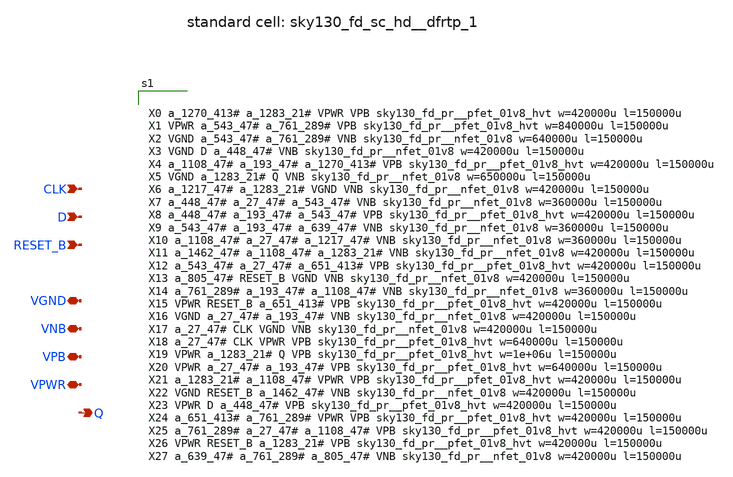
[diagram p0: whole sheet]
** sch_path: tt_um_mosbius/xschem/dff.sch
**.subckt dff CLK D RESET_B VGND VNB VPB VPWR Q
*.ipin CLK
*.ipin D
*.ipin RESET_B
*.iopin VGND
*.iopin VNB
*.iopin VPB
*.iopin VPWR
*.opin Q
**** begin user architecture code


X0 a_1270_413# a_1283_21# VPWR VPB sky130_fd_pr__pfet_01v8_hvt w=420000u l=150000u
X1 VPWR a_543_47# a_761_289# VPB sky130_fd_pr__pfet_01v8_hvt w=840000u l=150000u
X2 VGND a_543_47# a_761_289# VNB sky130_fd_pr__nfet_01v8 w=640000u l=150000u
X3 VGND D a_448_47# VNB sky130_fd_pr__nfet_01v8 w=420000u l=150000u
X4 a_1108_47# a_193_47# a_1270_413# VPB sky130_fd_pr__pfet_01v8_hvt w=420000u l=150000u
X5 VGND a_1283_21# Q VNB sky130_fd_pr__nfet_01v8 w=650000u l=150000u
X6 a_1217_47# a_1283_21# VGND VNB sky130_fd_pr__nfet_01v8 w=420000u l=150000u
X7 a_448_47# a_27_47# a_543_47# VNB sky130_fd_pr__nfet_01v8 w=360000u l=150000u
X8 a_448_47# a_193_47# a_543_47# VPB sky130_fd_pr__pfet_01v8_hvt w=420000u l=150000u
X9 a_543_47# a_193_47# a_639_47# VNB sky130_fd_pr__nfet_01v8 w=360000u l=150000u
X10 a_1108_47# a_27_47# a_1217_47# VNB sky130_fd_pr__nfet_01v8 w=360000u l=150000u
X11 a_1462_47# a_1108_47# a_1283_21# VNB sky130_fd_pr__nfet_01v8 w=420000u l=150000u
X12 a_543_47# a_27_47# a_651_413# VPB sky130_fd_pr__pfet_01v8_hvt w=420000u l=150000u
X13 a_805_47# RESET_B VGND VNB sky130_fd_pr__nfet_01v8 w=420000u l=150000u
X14 a_761_289# a_193_47# a_1108_47# VNB sky130_fd_pr__nfet_01v8 w=360000u l=150000u
X15 VPWR RESET_B a_651_413# VPB sky130_fd_pr__pfet_01v8_hvt w=420000u l=150000u
X16 VGND a_27_47# a_193_47# VNB sky130_fd_pr__nfet_01v8 w=420000u l=150000u
X17 a_27_47# CLK VGND VNB sky130_fd_pr__nfet_01v8 w=420000u l=150000u
X18 a_27_47# CLK VPWR VPB sky130_fd_pr__pfet_01v8_hvt w=640000u l=150000u
X19 VPWR a_1283_21# Q VPB sky130_fd_pr__pfet_01v8_hvt w=1e+06u l=150000u
X20 VPWR a_27_47# a_193_47# VPB sky130_fd_pr__pfet_01v8_hvt w=640000u l=150000u
X21 a_1283_21# a_1108_47# VPWR VPB sky130_fd_pr__pfet_01v8_hvt w=420000u l=150000u
X22 VGND RESET_B a_1462_47# VNB sky130_fd_pr__nfet_01v8 w=420000u l=150000u
X23 VPWR D a_448_47# VPB sky130_fd_pr__pfet_01v8_hvt w=420000u l=150000u
X24 a_651_413# a_761_289# VPWR VPB sky130_fd_pr__pfet_01v8_hvt w=420000u l=150000u
X25 a_761_289# a_27_47# a_1108_47# VPB sky130_fd_pr__pfet_01v8_hvt w=420000u l=150000u
X26 VPWR RESET_B a_1283_21# VPB sky130_fd_pr__pfet_01v8_hvt w=420000u l=150000u
X27 a_639_47# a_761_289# a_805_47# VNB sky130_fd_pr__nfet_01v8 w=420000u l=150000u




**** end user architecture code
**.ends
.end
